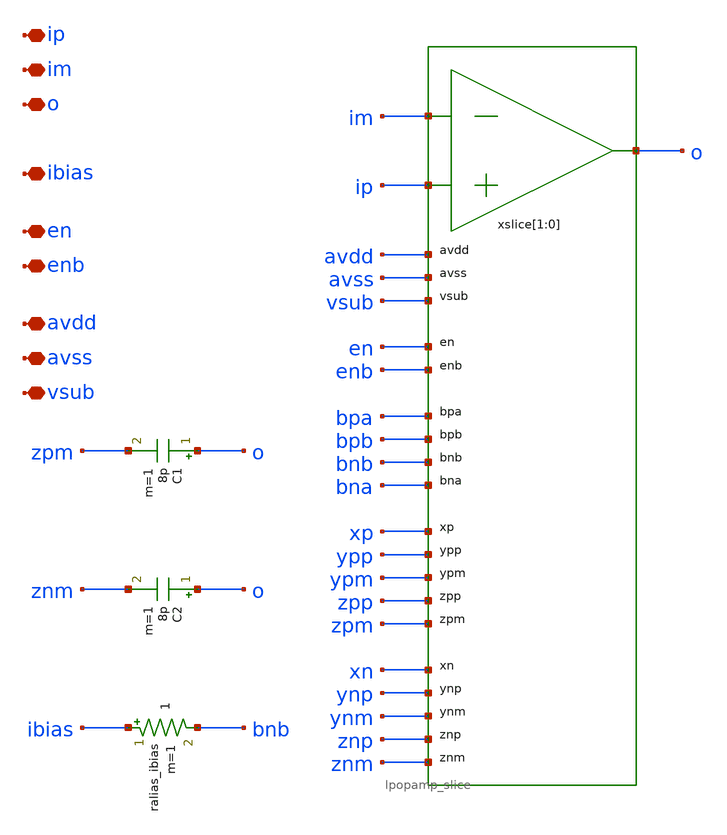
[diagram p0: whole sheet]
** sch_path: xschem/lpopamp_ref.sch
**.subckt lpopamp_ref avdd avss ip im o ibias en enb vsub
*.iopin avdd
*.iopin avss
*.iopin ip
*.iopin im
*.iopin o
*.iopin ibias
*.iopin en
*.iopin enb
*.iopin vsub
xslice[1] im ip o avdd avss en enb bpa bpb bnb bna xp ypp ypm zpp zpm xn ynp ynm znp znm
+ lpopamp_slice
xslice[0] im ip o avdd avss en enb bpa bpb bnb bna xp ypp ypm zpp zpm xn ynp ynm znp znm
+ lpopamp_slice
ralias_ibias ibias bnb 1 m=1
C1 o zpm 8p m=1
C2 o znm 8p m=1
**.ends
.end
